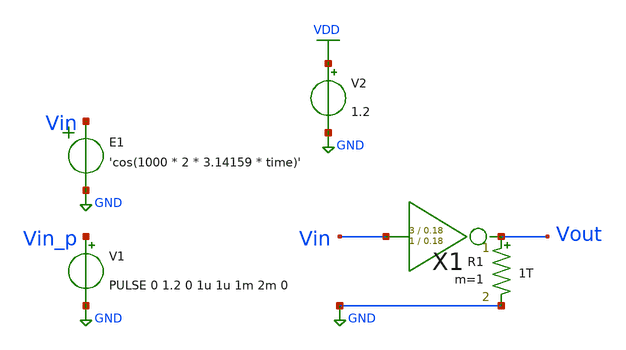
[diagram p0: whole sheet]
** sch_path: xschem/Switched_Caps/Inverter Test.sch
**.subckt Inverter Test
X1 Vin Vout inv Wpmos=3 Lpmos=0.18 Wnmos=1 Lnmos=0.18
V1 Vin_p GND PULSE 0 1.2 0 1u 1u 1m 2m 0
R1 Vout GND 1T m=1
V2 VDD GND 1.2
E1 Vin GND VOL=' 'cos(1000 * 2 * 3.14159 * time)' '
**** begin user architecture code


.lib /home/sky/sky130A/libs.tech/ngspice/sky130.lib.spice tt
.options abstol=1e-14 reltol=1e-4
.tran 50u 50m
.save all


**** end user architecture code
**.ends

* expanding   symbol:  inv/inv.sym # of pins=2
** sym_path: xschem/inv/inv.sym
** sch_path: xschem/inv/inv.sch
.subckt inv in out  Wpmos=3 Lpmos=0.18 Wnmos=1 Lnmos=0.18
*.ipin in
*.iopin out
XM1 out in GND GND sky130_fd_pr__nfet_01v8 L=Lnmos W=Wnmos nf=1 ad='int((nf+1)/2) * W/nf * 0.29' as='int((nf+2)/2) * W/nf * 0.29'
+ pd='2*int((nf+1)/2) * (W/nf + 0.29)' ps='2*int((nf+2)/2) * (W/nf + 0.29)' nrd='0.29 / W' nrs='0.29 / W'
+ sa=0 sb=0 sd=0 mult=1 m=1
XM2 out in VDD VDD sky130_fd_pr__pfet_01v8 L=Lpmos W=Wpmos nf=1 ad='int((nf+1)/2) * W/nf * 0.29' as='int((nf+2)/2) * W/nf * 0.29'
+ pd='2*int((nf+1)/2) * (W/nf + 0.29)' ps='2*int((nf+2)/2) * (W/nf + 0.29)' nrd='0.29 / W' nrs='0.29 / W'
+ sa=0 sb=0 sd=0 mult=1 m=1
.ends

.GLOBAL GND
.GLOBAL VDD
.end
